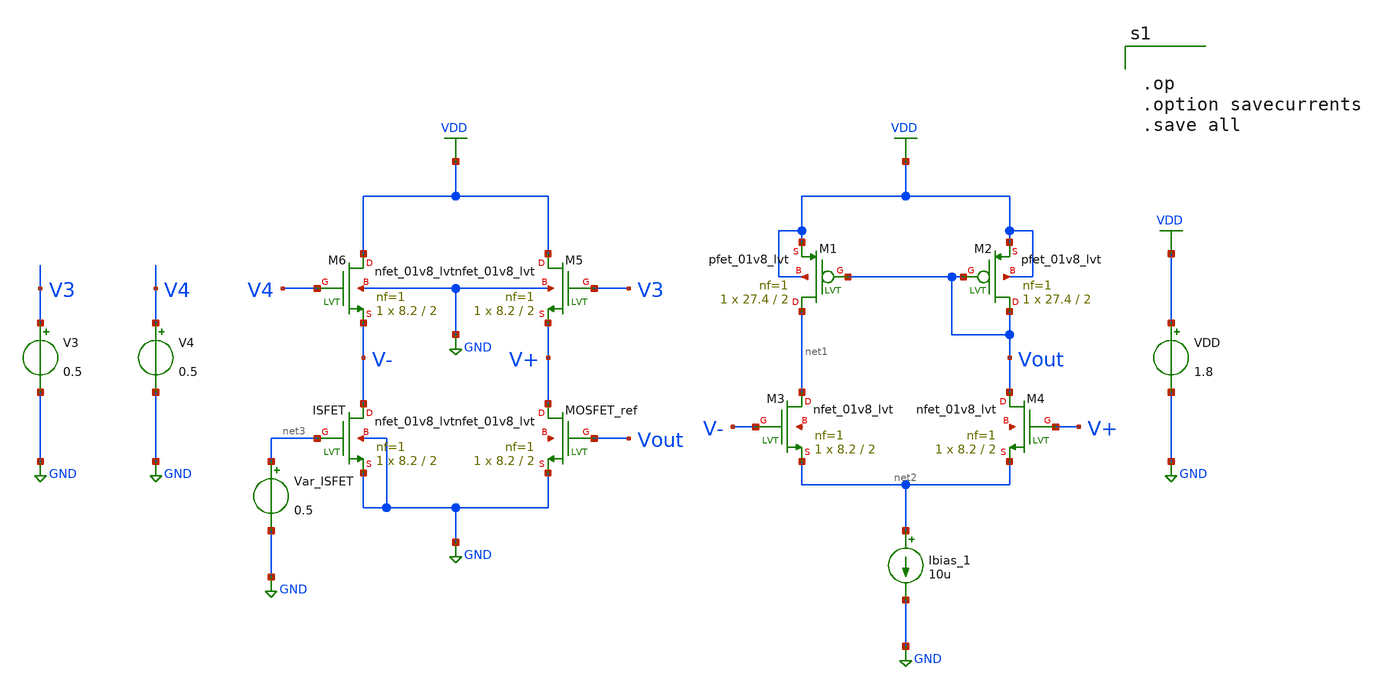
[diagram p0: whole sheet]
** sch_path: Pont_Wheatstone.sch
**.subckt Pont_Wheatstone
XM2 Vout Vout VDD VDD sky130_fd_pr__pfet_01v8_lvt L=2 W=27.4 nf=1 ad='int((nf+1)/2) * W/nf * 0.29' as='int((nf+2)/2) * W/nf * 0.29'
+ pd='2*int((nf+1)/2) * (W/nf + 0.29)' ps='2*int((nf+2)/2) * (W/nf + 0.29)' nrd='0.29 / W' nrs='0.29 / W'
+ sa=0 sb=0 sd=0 mult=1 m=1
XM3 net1 V- net2 net4 sky130_fd_pr__nfet_01v8_lvt L=2 W=8.2 nf=1 ad='int((nf+1)/2) * W/nf * 0.29' as='int((nf+2)/2) * W/nf * 0.29'
+ pd='2*int((nf+1)/2) * (W/nf + 0.29)' ps='2*int((nf+2)/2) * (W/nf + 0.29)' nrd='0.29 / W' nrs='0.29 / W'
+ sa=0 sb=0 sd=0 mult=1 m=1
VDD VDD GND 1.8
XM1 net1 Vout VDD VDD sky130_fd_pr__pfet_01v8_lvt L=2 W=27.4 nf=1 ad='int((nf+1)/2) * W/nf * 0.29' as='int((nf+2)/2) * W/nf * 0.29'
+ pd='2*int((nf+1)/2) * (W/nf + 0.29)' ps='2*int((nf+2)/2) * (W/nf + 0.29)' nrd='0.29 / W' nrs='0.29 / W'
+ sa=0 sb=0 sd=0 mult=1 m=1
XM4 Vout V+ net2 net5 sky130_fd_pr__nfet_01v8_lvt L=2 W=8.2 nf=1 ad='int((nf+1)/2) * W/nf * 0.29' as='int((nf+2)/2) * W/nf * 0.29'
+ pd='2*int((nf+1)/2) * (W/nf + 0.29)' ps='2*int((nf+2)/2) * (W/nf + 0.29)' nrd='0.29 / W' nrs='0.29 / W'
+ sa=0 sb=0 sd=0 mult=1 m=1
Ibias_1 net2 GND 10u
XM5 VDD V3 V+ GND sky130_fd_pr__nfet_01v8_lvt L=2 W=8.2 nf=1 ad='int((nf+1)/2) * W/nf * 0.29' as='int((nf+2)/2) * W/nf * 0.29'
+ pd='2*int((nf+1)/2) * (W/nf + 0.29)' ps='2*int((nf+2)/2) * (W/nf + 0.29)' nrd='0.29 / W' nrs='0.29 / W'
+ sa=0 sb=0 sd=0 mult=1 m=1
XM6 VDD V4 V- GND sky130_fd_pr__nfet_01v8_lvt L=2 W=8.2 nf=1 ad='int((nf+1)/2) * W/nf * 0.29' as='int((nf+2)/2) * W/nf * 0.29'
+ pd='2*int((nf+1)/2) * (W/nf + 0.29)' ps='2*int((nf+2)/2) * (W/nf + 0.29)' nrd='0.29 / W' nrs='0.29 / W'
+ sa=0 sb=0 sd=0 mult=1 m=1
XMOSFET_ref V+ Vout GND net6 sky130_fd_pr__nfet_01v8_lvt L=2 W=8.2 nf=1 ad='int((nf+1)/2) * W/nf * 0.29'
+ as='int((nf+2)/2) * W/nf * 0.29' pd='2*int((nf+1)/2) * (W/nf + 0.29)' ps='2*int((nf+2)/2) * (W/nf + 0.29)'
+ nrd='0.29 / W' nrs='0.29 / W' sa=0 sb=0 sd=0 mult=1 m=1
XISFET V- net3 GND GND sky130_fd_pr__nfet_01v8_lvt L=2 W=8.2 nf=1 ad='int((nf+1)/2) * W/nf * 0.29' as='int((nf+2)/2) * W/nf * 0.29'
+ pd='2*int((nf+1)/2) * (W/nf + 0.29)' ps='2*int((nf+2)/2) * (W/nf + 0.29)' nrd='0.29 / W' nrs='0.29 / W'
+ sa=0 sb=0 sd=0 mult=1 m=1
Var_ISFET net3 GND 0.5
V3 V3 GND 0.5
V4 V4 GND 0.5
**** begin user architecture code

** opencircuitdesign pdks install
.lib $::SKYWATER_MODELS/sky130.lib.spice tt



.op
.option savecurrents
.save all

**** end user architecture code
**.ends
.GLOBAL GND
.GLOBAL VDD
.end
